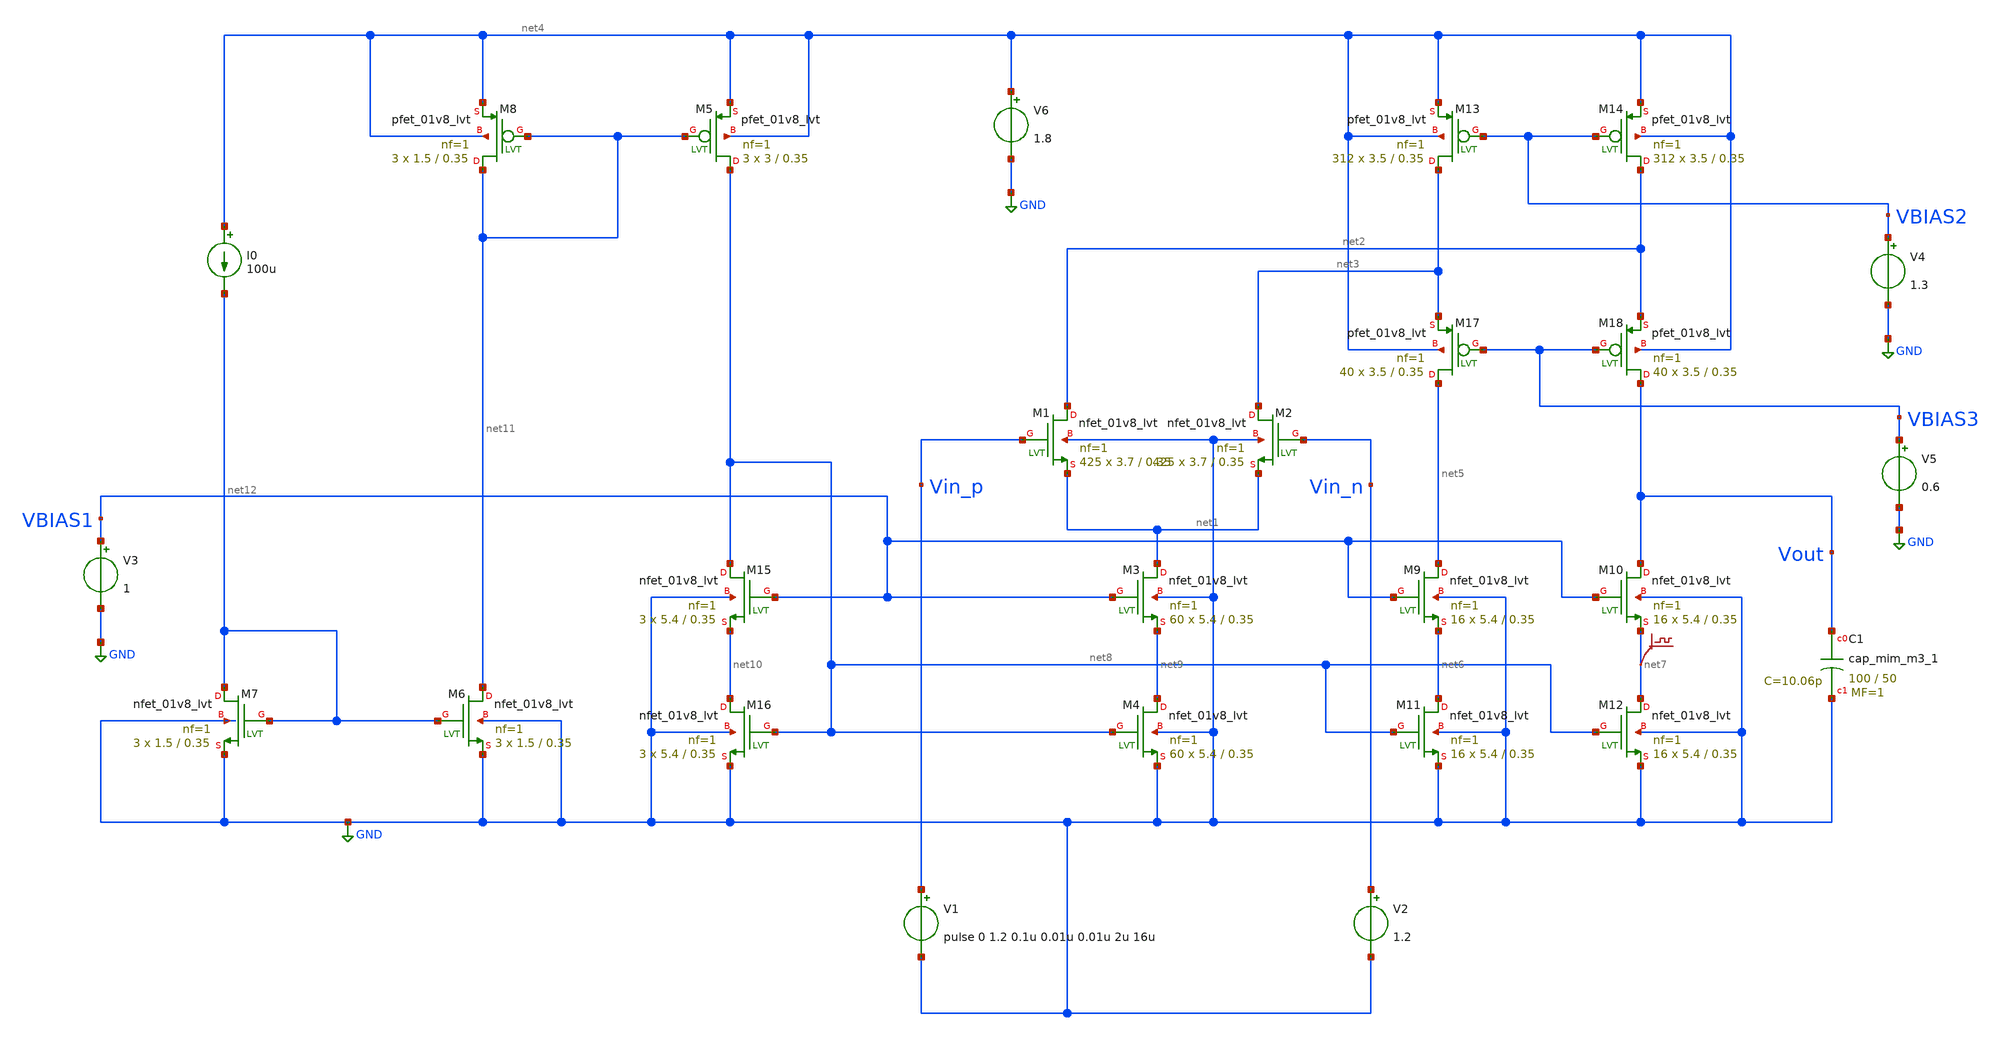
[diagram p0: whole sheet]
** sch_path: xschem/ip_block/opamp/folded_cas_xiaoyi/OTA-1.0.sch
**.subckt OTA-1.0
XM1 net2 Vin_p net1 GND sky130_fd_pr__nfet_01v8_lvt L=0.35 W=3.7 nf=1 ad='int((nf+1)/2) * W/nf * 0.29'
+ as='int((nf+2)/2) * W/nf * 0.29' pd='2*int((nf+1)/2) * (W/nf + 0.29)' ps='2*int((nf+2)/2) * (W/nf + 0.29)'
+ nrd='0.29 / W' nrs='0.29 / W' sa=0 sb=0 sd=0 mult=425 m=425
XM2 net3 Vin_n net1 GND sky130_fd_pr__nfet_01v8_lvt L=0.35 W=3.7 nf=1 ad='int((nf+1)/2) * W/nf * 0.29'
+ as='int((nf+2)/2) * W/nf * 0.29' pd='2*int((nf+1)/2) * (W/nf + 0.29)' ps='2*int((nf+2)/2) * (W/nf + 0.29)'
+ nrd='0.29 / W' nrs='0.29 / W' sa=0 sb=0 sd=0 mult=425 m=425
XM3 net1 VBIAS1 net9 GND sky130_fd_pr__nfet_01v8_lvt L=0.35 W=5.4 nf=1 ad='int((nf+1)/2) * W/nf * 0.29'
+ as='int((nf+2)/2) * W/nf * 0.29' pd='2*int((nf+1)/2) * (W/nf + 0.29)' ps='2*int((nf+2)/2) * (W/nf + 0.29)'
+ nrd='0.29 / W' nrs='0.29 / W' sa=0 sb=0 sd=0 mult=60 m=60
XM4 net9 net8 GND GND sky130_fd_pr__nfet_01v8_lvt L=0.35 W=5.4 nf=1 ad='int((nf+1)/2) * W/nf * 0.29'
+ as='int((nf+2)/2) * W/nf * 0.29' pd='2*int((nf+1)/2) * (W/nf + 0.29)' ps='2*int((nf+2)/2) * (W/nf + 0.29)'
+ nrd='0.29 / W' nrs='0.29 / W' sa=0 sb=0 sd=0 mult=60 m=60
XM9 net5 VBIAS1 net6 GND sky130_fd_pr__nfet_01v8_lvt L=0.35 W=5.4 nf=1 ad='int((nf+1)/2) * W/nf * 0.29'
+ as='int((nf+2)/2) * W/nf * 0.29' pd='2*int((nf+1)/2) * (W/nf + 0.29)' ps='2*int((nf+2)/2) * (W/nf + 0.29)'
+ nrd='0.29 / W' nrs='0.29 / W' sa=0 sb=0 sd=0 mult=16 m=16
XM10 Vout VBIAS1 net7 GND sky130_fd_pr__nfet_01v8_lvt L=0.35 W=5.4 nf=1 ad='int((nf+1)/2) * W/nf * 0.29'
+ as='int((nf+2)/2) * W/nf * 0.29' pd='2*int((nf+1)/2) * (W/nf + 0.29)' ps='2*int((nf+2)/2) * (W/nf + 0.29)'
+ nrd='0.29 / W' nrs='0.29 / W' sa=0 sb=0 sd=0 mult=16 m=16
XM11 net6 net8 GND GND sky130_fd_pr__nfet_01v8_lvt L=0.35 W=5.4 nf=1 ad='int((nf+1)/2) * W/nf * 0.29'
+ as='int((nf+2)/2) * W/nf * 0.29' pd='2*int((nf+1)/2) * (W/nf + 0.29)' ps='2*int((nf+2)/2) * (W/nf + 0.29)'
+ nrd='0.29 / W' nrs='0.29 / W' sa=0 sb=0 sd=0 mult=16 m=16
XM12 net7 net8 GND GND sky130_fd_pr__nfet_01v8_lvt L=0.35 W=5.4 nf=1 ad='int((nf+1)/2) * W/nf * 0.29'
+ as='int((nf+2)/2) * W/nf * 0.29' pd='2*int((nf+1)/2) * (W/nf + 0.29)' ps='2*int((nf+2)/2) * (W/nf + 0.29)'
+ nrd='0.29 / W' nrs='0.29 / W' sa=0 sb=0 sd=0 mult=16 m=16
V1 Vin_p GND pulse 0 1.2 0.1u 0.01u 0.01u 2u 16u
V2 Vin_n GND 1.2
XM15 net8 VBIAS1 net10 GND sky130_fd_pr__nfet_01v8_lvt L=0.35 W=5.4 nf=1 ad='int((nf+1)/2) * W/nf * 0.29'
+ as='int((nf+2)/2) * W/nf * 0.29' pd='2*int((nf+1)/2) * (W/nf + 0.29)' ps='2*int((nf+2)/2) * (W/nf + 0.29)'
+ nrd='0.29 / W' nrs='0.29 / W' sa=0 sb=0 sd=0 mult=3 m=3
XM16 net10 net8 GND GND sky130_fd_pr__nfet_01v8_lvt L=0.35 W=5.4 nf=1 ad='int((nf+1)/2) * W/nf * 0.29'
+ as='int((nf+2)/2) * W/nf * 0.29' pd='2*int((nf+1)/2) * (W/nf + 0.29)' ps='2*int((nf+2)/2) * (W/nf + 0.29)'
+ nrd='0.29 / W' nrs='0.29 / W' sa=0 sb=0 sd=0 mult=3 m=3
XM6 net11 net12 GND GND sky130_fd_pr__nfet_01v8_lvt L=0.35 W=1.5 nf=1 ad='int((nf+1)/2) * W/nf * 0.29'
+ as='int((nf+2)/2) * W/nf * 0.29' pd='2*int((nf+1)/2) * (W/nf + 0.29)' ps='2*int((nf+2)/2) * (W/nf + 0.29)'
+ nrd='0.29 / W' nrs='0.29 / W' sa=0 sb=0 sd=0 mult=3 m=3
XM7 net12 net12 GND GND sky130_fd_pr__nfet_01v8_lvt L=0.35 W=1.5 nf=1 ad='int((nf+1)/2) * W/nf * 0.29'
+ as='int((nf+2)/2) * W/nf * 0.29' pd='2*int((nf+1)/2) * (W/nf + 0.29)' ps='2*int((nf+2)/2) * (W/nf + 0.29)'
+ nrd='0.29 / W' nrs='0.29 / W' sa=0 sb=0 sd=0 mult=3 m=3
I0 net4 net12 100u
V3 VBIAS1 GND 1
V4 VBIAS2 GND 1.3
V5 VBIAS3 GND 0.6
.save v(net7)
V6 net4 GND 1.8
XM8 net11 net11 net4 net4 sky130_fd_pr__pfet_01v8_lvt L=0.35 W=1.5 nf=1 ad='int((nf+1)/2) * W/nf * 0.29'
+ as='int((nf+2)/2) * W/nf * 0.29' pd='2*int((nf+1)/2) * (W/nf + 0.29)' ps='2*int((nf+2)/2) * (W/nf + 0.29)'
+ nrd='0.29 / W' nrs='0.29 / W' sa=0 sb=0 sd=0 mult=3 m=3
XM5 net8 net11 net4 net4 sky130_fd_pr__pfet_01v8_lvt L=0.35 W=3 nf=1 ad='int((nf+1)/2) * W/nf * 0.29'
+ as='int((nf+2)/2) * W/nf * 0.29' pd='2*int((nf+1)/2) * (W/nf + 0.29)' ps='2*int((nf+2)/2) * (W/nf + 0.29)'
+ nrd='0.29 / W' nrs='0.29 / W' sa=0 sb=0 sd=0 mult=3 m=3
XM13 net3 VBIAS2 net4 net4 sky130_fd_pr__pfet_01v8_lvt L=0.35 W=3.5 nf=1 ad='int((nf+1)/2) * W/nf * 0.29'
+ as='int((nf+2)/2) * W/nf * 0.29' pd='2*int((nf+1)/2) * (W/nf + 0.29)' ps='2*int((nf+2)/2) * (W/nf + 0.29)'
+ nrd='0.29 / W' nrs='0.29 / W' sa=0 sb=0 sd=0 mult=312 m=312
XM14 net2 VBIAS2 net4 net4 sky130_fd_pr__pfet_01v8_lvt L=0.35 W=3.5 nf=1 ad='int((nf+1)/2) * W/nf * 0.29'
+ as='int((nf+2)/2) * W/nf * 0.29' pd='2*int((nf+1)/2) * (W/nf + 0.29)' ps='2*int((nf+2)/2) * (W/nf + 0.29)'
+ nrd='0.29 / W' nrs='0.29 / W' sa=0 sb=0 sd=0 mult=312 m=312
XM17 net5 VBIAS3 net3 net4 sky130_fd_pr__pfet_01v8_lvt L=0.35 W=3.5 nf=1 ad='int((nf+1)/2) * W/nf * 0.29'
+ as='int((nf+2)/2) * W/nf * 0.29' pd='2*int((nf+1)/2) * (W/nf + 0.29)' ps='2*int((nf+2)/2) * (W/nf + 0.29)'
+ nrd='0.29 / W' nrs='0.29 / W' sa=0 sb=0 sd=0 mult=40 m=40
XM18 Vout VBIAS3 net2 net4 sky130_fd_pr__pfet_01v8_lvt L=0.35 W=3.5 nf=1 ad='int((nf+1)/2) * W/nf * 0.29'
+ as='int((nf+2)/2) * W/nf * 0.29' pd='2*int((nf+1)/2) * (W/nf + 0.29)' ps='2*int((nf+2)/2) * (W/nf + 0.29)'
+ nrd='0.29 / W' nrs='0.29 / W' sa=0 sb=0 sd=0 mult=40 m=40
XC1 Vout GND sky130_fd_pr__cap_mim_m3_1 W=100 L=50 MF=1 m=1
**** begin user architecture code

** opencircuitdesign pdks install
.lib $::SKYWATER_MODELS/sky130.lib.spice tt




.option temp=27

*.op
*.ac dec 10 1 1G
*.tran 0.001 0.2u 10n

.control
save all
run
*ac dec 10 1 1G
tran 1u 10u
display
ac dec 10 1 1G
*let phase = 180/PI*vp(Vout)

*plot vdb(Vout) phase
plot Vin_p Vout
.endc

.save all



**** end user architecture code
**.ends
.GLOBAL GND
.end
